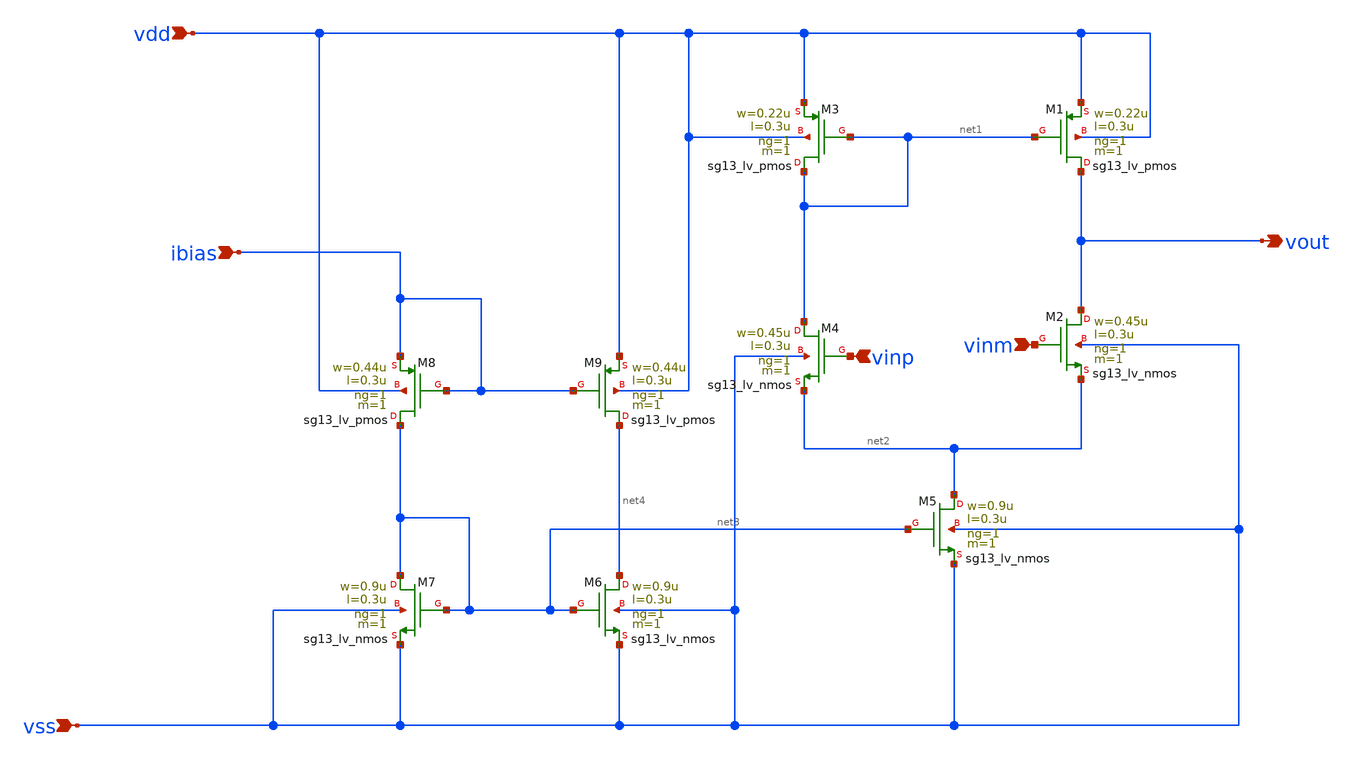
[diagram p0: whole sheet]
** sch_path: design/ota_design/trail2-ota5.sch
**.subckt trail2-ota5 vss vdd ibias vinm vinp vout
*.ipin vss
*.ipin vdd
*.ipin ibias
*.ipin vinm
*.ipin vinp
*.opin vout
XM1 vout net1 vdd vdd sg13_lv_pmos w=0.22u l=0.3u ng=1 m=1 mm_ok=1
XM2 vout vinm net2 vss sg13_lv_nmos w=0.45u l=0.3u ng=1 m=1 mm_ok=1
XM3 net1 net1 vdd vdd sg13_lv_pmos w=0.22u l=0.3u ng=1 m=1 mm_ok=1
XM4 net1 vinp net2 vss sg13_lv_nmos w=0.45u l=0.3u ng=1 m=1 mm_ok=1
XM5 net2 net3 vss vss sg13_lv_nmos w=0.9u l=0.3u ng=1 m=1 mm_ok=1
XM6 net4 net3 vss vss sg13_lv_nmos w=0.9u l=0.3u ng=1 m=1 mm_ok=1
XM7 net3 net3 vss vss sg13_lv_nmos w=0.9u l=0.3u ng=1 m=1 mm_ok=1
XM8 net3 ibias ibias vdd sg13_lv_pmos w=0.44u l=0.3u ng=1 m=1 mm_ok=1
XM9 net4 ibias vdd vdd sg13_lv_pmos w=0.44u l=0.3u ng=1 m=1 mm_ok=1
**.ends
.end
